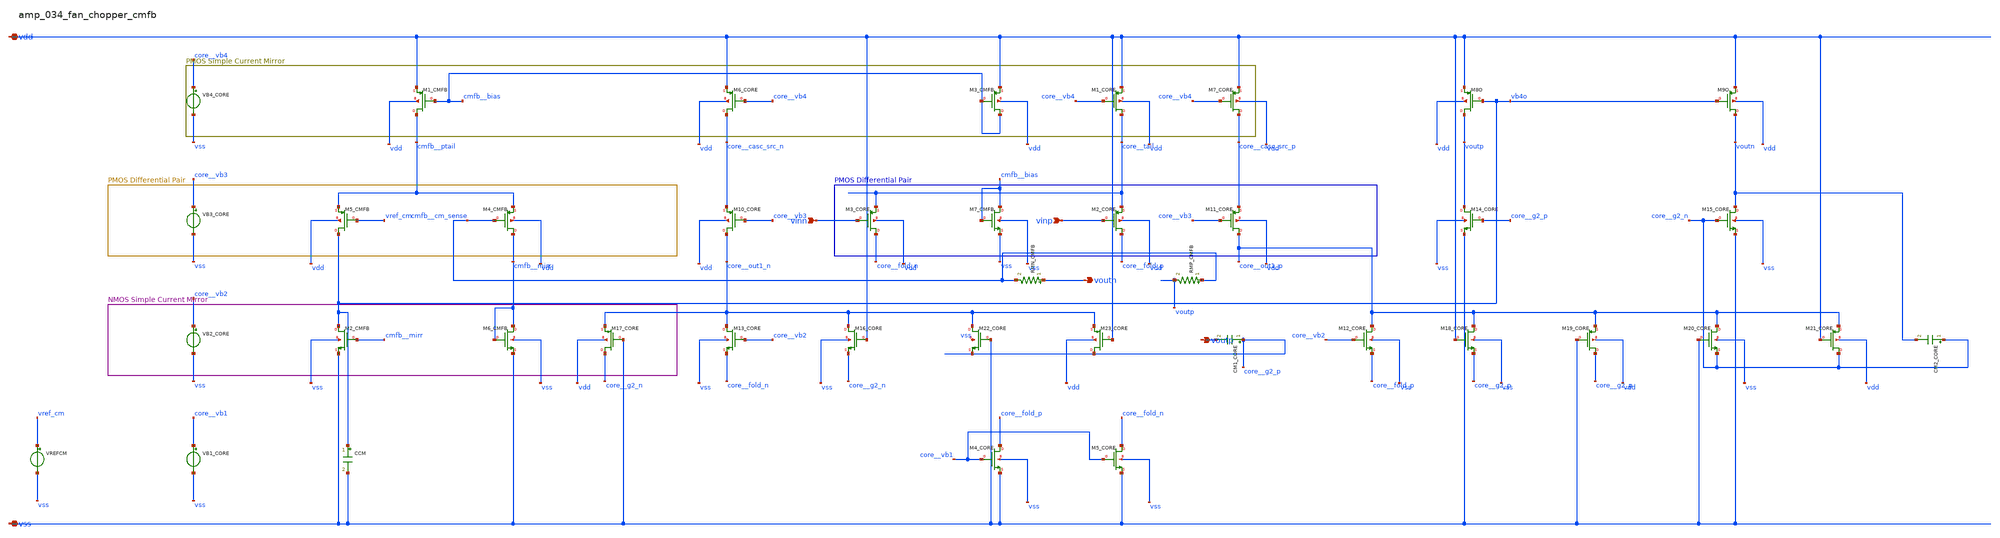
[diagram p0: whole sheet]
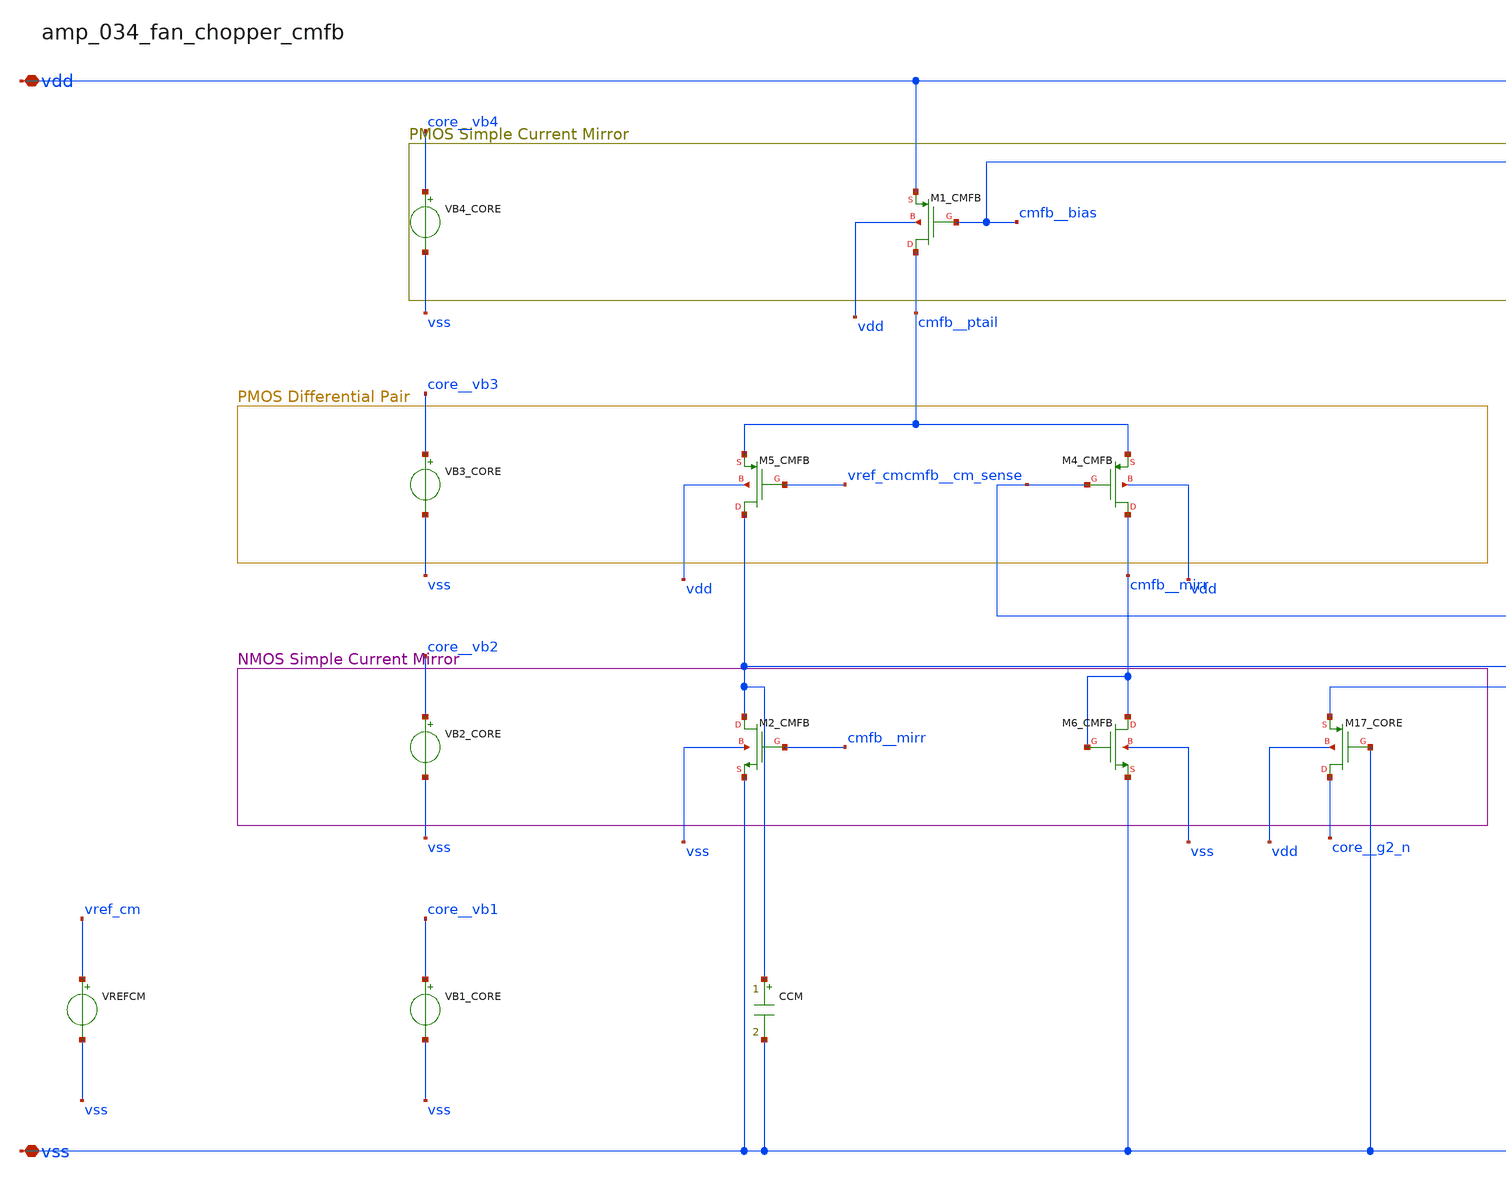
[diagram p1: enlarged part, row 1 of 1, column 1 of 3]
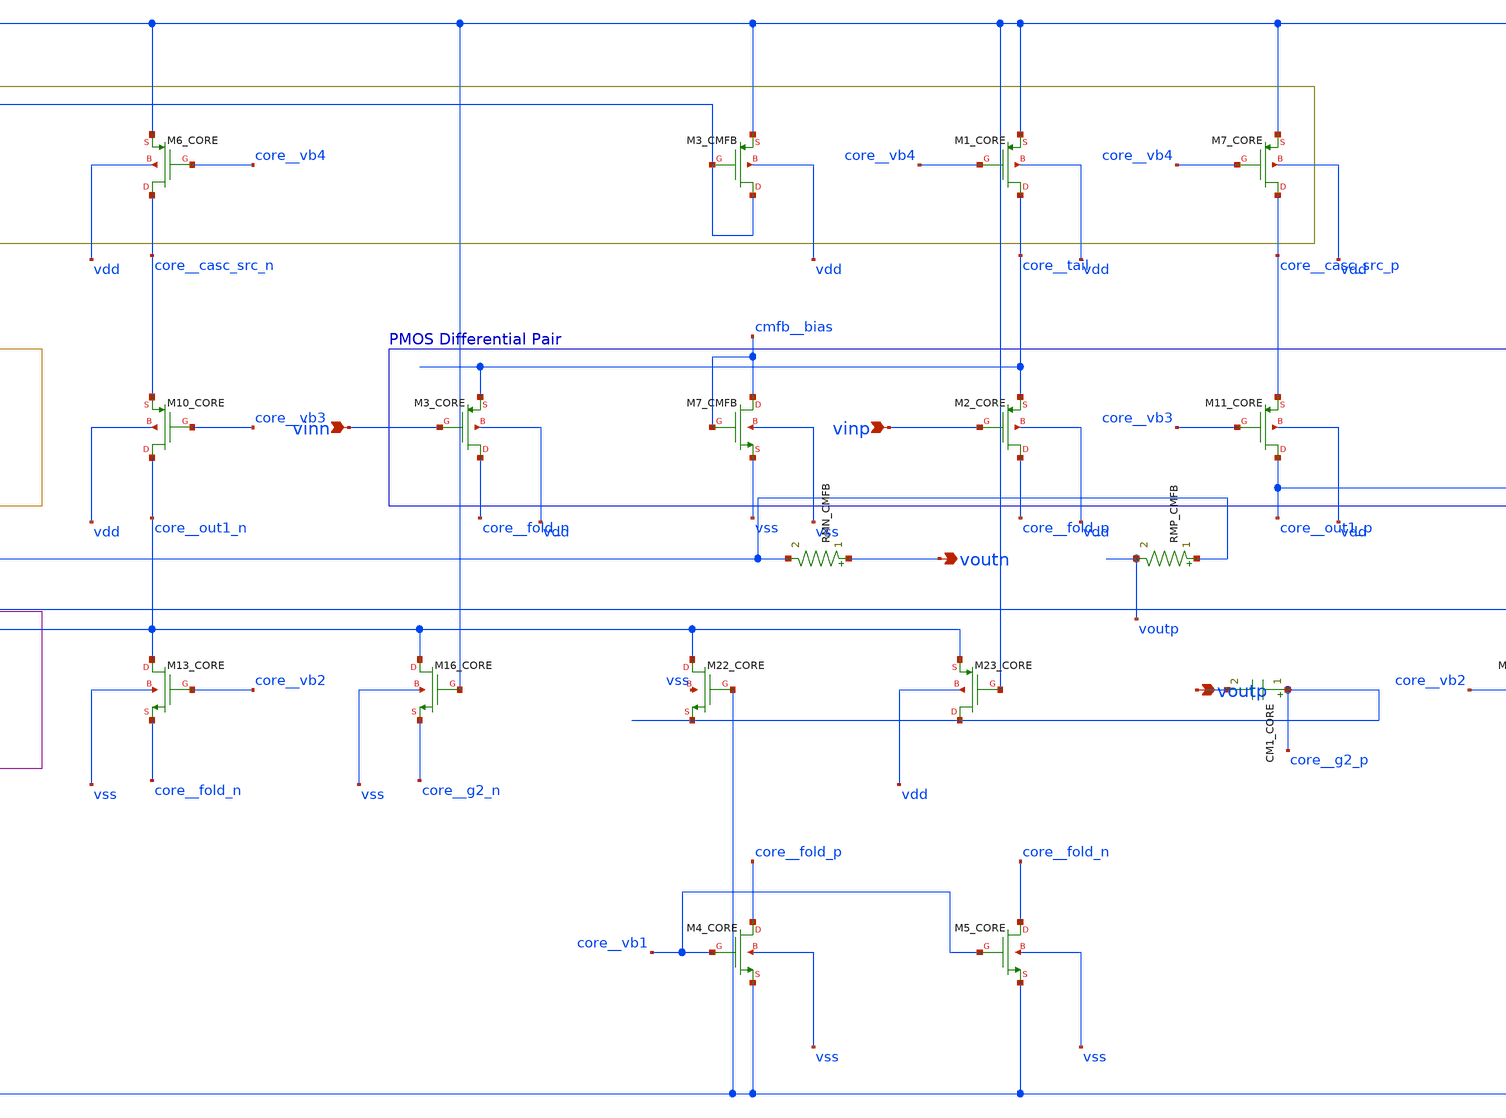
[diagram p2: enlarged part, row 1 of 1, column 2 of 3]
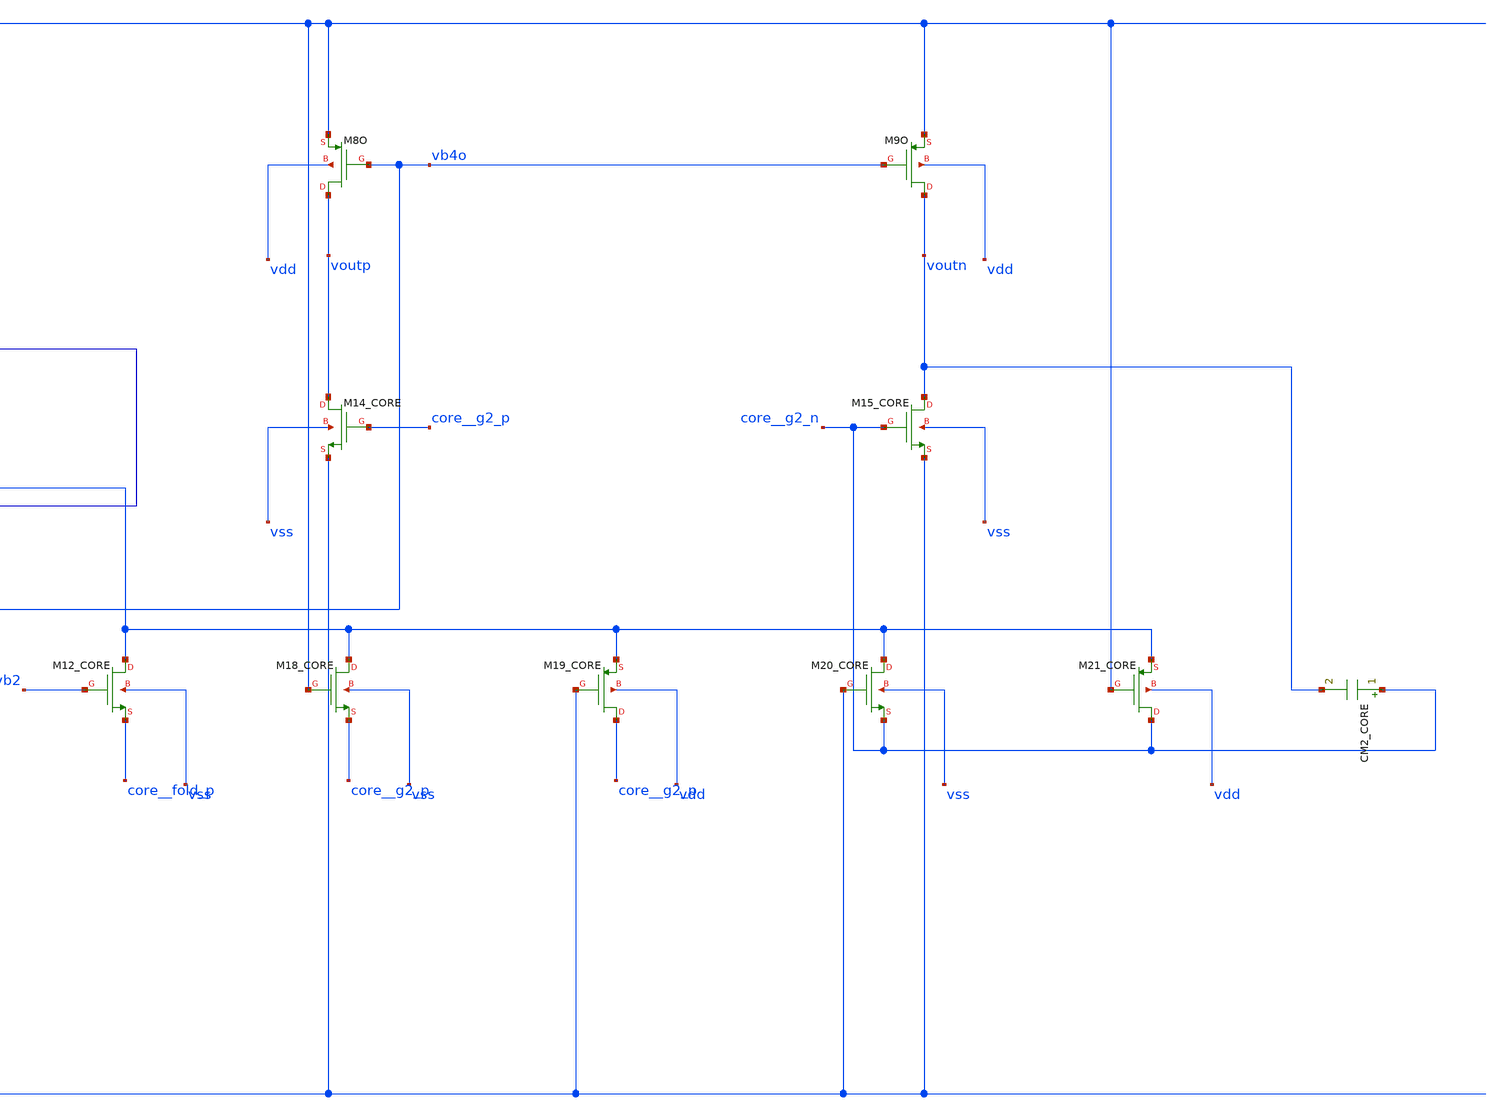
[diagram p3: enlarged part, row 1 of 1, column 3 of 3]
** sch_path: analog-db/raw/amp_034_fan_chopper_cmfb/amp_034_fan_chopper_cmfb_annotated.sch
**.subckt amp_034_fan_chopper_cmfb_annotated vinn vinp vdd vss voutp voutn
*.ipin vinn
*.ipin vinp
*.iopin vdd
*.iopin vss
*.opin voutp
*.opin voutn
CCM vb4o vss 'c_cm' m=1
CM1_CORE core__g2_p voutp 'x_dut_cm1_core_value' m=1
CM2_CORE core__g2_n voutn 'x_dut_cm2_core_value' m=1
RMN_CMFB voutn cmfb__cm_sense 'x_dut_rmn_cmfb_value' m=1
RMP_CMFB cmfb__cm_sense voutp 'x_dut_rmp_cmfb_value' m=1
VB1_CORE core__vb1 vss dc {vb1_core}
VB2_CORE core__vb2 vss dc {vb2_core}
VB3_CORE core__vb3 vss dc {vb3_core}
VB4_CORE core__vb4 vss dc {vb4_core}
VREFCM vref_cm vss dc {vcm_ref}
XM10_CORE core__out1_n core__vb3 core__casc_src_n vdd sg13_lv_pmos w=x_dut_xm10_core_w
+ l=x_dut_xm10_core_l ng=1 m=x_dut_xm10_core_m
XM11_CORE core__out1_p core__vb3 core__casc_src_p vdd sg13_lv_pmos w=x_dut_xm11_core_w
+ l=x_dut_xm11_core_l ng=1 m=x_dut_xm11_core_m
XM12_CORE core__out1_p core__vb2 core__fold_p vss sg13_lv_nmos w=x_dut_xm12_core_w
+ l=x_dut_xm12_core_l ng=1 m=x_dut_xm12_core_m
XM13_CORE core__out1_n core__vb2 core__fold_n vss sg13_lv_nmos w=x_dut_xm13_core_w
+ l=x_dut_xm13_core_l ng=1 m=x_dut_xm13_core_m
XM14_CORE voutp core__g2_p vss vss sg13_lv_nmos w=x_dut_xm14_core_w l=x_dut_xm14_core_l ng=1
+ m=x_dut_xm14_core_m
XM15_CORE voutn core__g2_n vss vss sg13_lv_nmos w=x_dut_xm15_core_w l=x_dut_xm15_core_l ng=1
+ m=x_dut_xm15_core_m
XM16_CORE core__out1_n vdd core__g2_n vss sg13_lv_nmos w=x_dut_xm16_core_w l=x_dut_xm16_core_l ng=1
+ m=x_dut_xm16_core_m
XM17_CORE core__g2_n vss core__out1_n vdd sg13_lv_pmos w=x_dut_xm17_core_w l=x_dut_xm17_core_l ng=1
+ m=x_dut_xm17_core_m
XM18_CORE core__out1_p vdd core__g2_p vss sg13_lv_nmos w=x_dut_xm18_core_w l=x_dut_xm18_core_l ng=1
+ m=x_dut_xm18_core_m
XM19_CORE core__g2_p vss core__out1_p vdd sg13_lv_pmos w=x_dut_xm19_core_w l=x_dut_xm19_core_l ng=1
+ m=x_dut_xm19_core_m
XM1_CMFB cmfb__ptail cmfb__bias vdd vdd sg13_lv_pmos w=x_dut_xm1_cmfb_w l=x_dut_xm1_cmfb_l ng=1
+ m=x_dut_xm1_cmfb_m
XM1_CORE core__tail core__vb4 vdd vdd sg13_lv_pmos w=x_dut_xm1_core_w l=x_dut_xm1_core_l ng=1
+ m=x_dut_xm1_core_m
XM20_CORE core__out1_p vss core__g2_n vss sg13_lv_nmos w=x_dut_xm20_core_w l=x_dut_xm20_core_l ng=1
+ m=x_dut_xm20_core_m
XM21_CORE core__g2_n vdd core__out1_p vdd sg13_lv_pmos w=x_dut_xm21_core_w l=x_dut_xm21_core_l ng=1
+ m=x_dut_xm21_core_m
XM22_CORE core__out1_n vss core__g2_p vss sg13_lv_nmos w=x_dut_xm22_core_w l=x_dut_xm22_core_l ng=1
+ m=x_dut_xm22_core_m
XM23_CORE core__g2_p vdd core__out1_n vdd sg13_lv_pmos w=x_dut_xm23_core_w l=x_dut_xm23_core_l ng=1
+ m=x_dut_xm23_core_m
XM2_CMFB vb4o cmfb__mirr vss vss sg13_lv_nmos w=x_dut_xm2_cmfb_w l=x_dut_xm2_cmfb_l ng=1
+ m=x_dut_xm2_cmfb_m
XM2_CORE core__fold_p vinp core__tail vdd sg13_lv_pmos w=x_dut_xm2_core_w l=x_dut_xm2_core_l ng=1
+ m=x_dut_xm2_core_m
XM3_CMFB cmfb__bias cmfb__bias vdd vdd sg13_lv_pmos w=x_dut_xm3_cmfb_w l=x_dut_xm3_cmfb_l ng=1
+ m=x_dut_xm3_cmfb_m
XM3_CORE core__fold_n vinn core__tail vdd sg13_lv_pmos w=x_dut_xm3_core_w l=x_dut_xm3_core_l ng=1
+ m=x_dut_xm3_core_m
XM4_CMFB cmfb__mirr cmfb__cm_sense cmfb__ptail vdd sg13_lv_pmos w=x_dut_xm4_cmfb_w
+ l=x_dut_xm4_cmfb_l ng=1 m=x_dut_xm4_cmfb_m
XM4_CORE core__fold_p core__vb1 vss vss sg13_lv_nmos w=x_dut_xm4_core_w l=x_dut_xm4_core_l ng=1
+ m=x_dut_xm4_core_m
XM5_CMFB vb4o vref_cm cmfb__ptail vdd sg13_lv_pmos w=x_dut_xm5_cmfb_w l=x_dut_xm5_cmfb_l ng=1
+ m=x_dut_xm5_cmfb_m
XM5_CORE core__fold_n core__vb1 vss vss sg13_lv_nmos w=x_dut_xm5_core_w l=x_dut_xm5_core_l ng=1
+ m=x_dut_xm5_core_m
XM6_CMFB cmfb__mirr cmfb__mirr vss vss sg13_lv_nmos w=x_dut_xm6_cmfb_w l=x_dut_xm6_cmfb_l ng=1
+ m=x_dut_xm6_cmfb_m
XM6_CORE core__casc_src_n core__vb4 vdd vdd sg13_lv_pmos w=x_dut_xm6_core_w l=x_dut_xm6_core_l ng=1
+ m=x_dut_xm6_core_m
XM7_CMFB cmfb__bias cmfb__bias vss vss sg13_lv_nmos w=x_dut_xm7_cmfb_w l=x_dut_xm7_cmfb_l ng=1
+ m=x_dut_xm7_cmfb_m
XM7_CORE core__casc_src_p core__vb4 vdd vdd sg13_lv_pmos w=x_dut_xm7_core_w l=x_dut_xm7_core_l ng=1
+ m=x_dut_xm7_core_m
XM8O voutp vb4o vdd vdd sg13_lv_pmos w=x_dut_xm8o_w l=x_dut_xm8o_l ng=1 m=x_dut_xm8o_m
XM9O voutn vb4o vdd vdd sg13_lv_pmos w=x_dut_xm9o_w l=x_dut_xm9o_l ng=1 m=x_dut_xm9o_m
**.ends
.end
